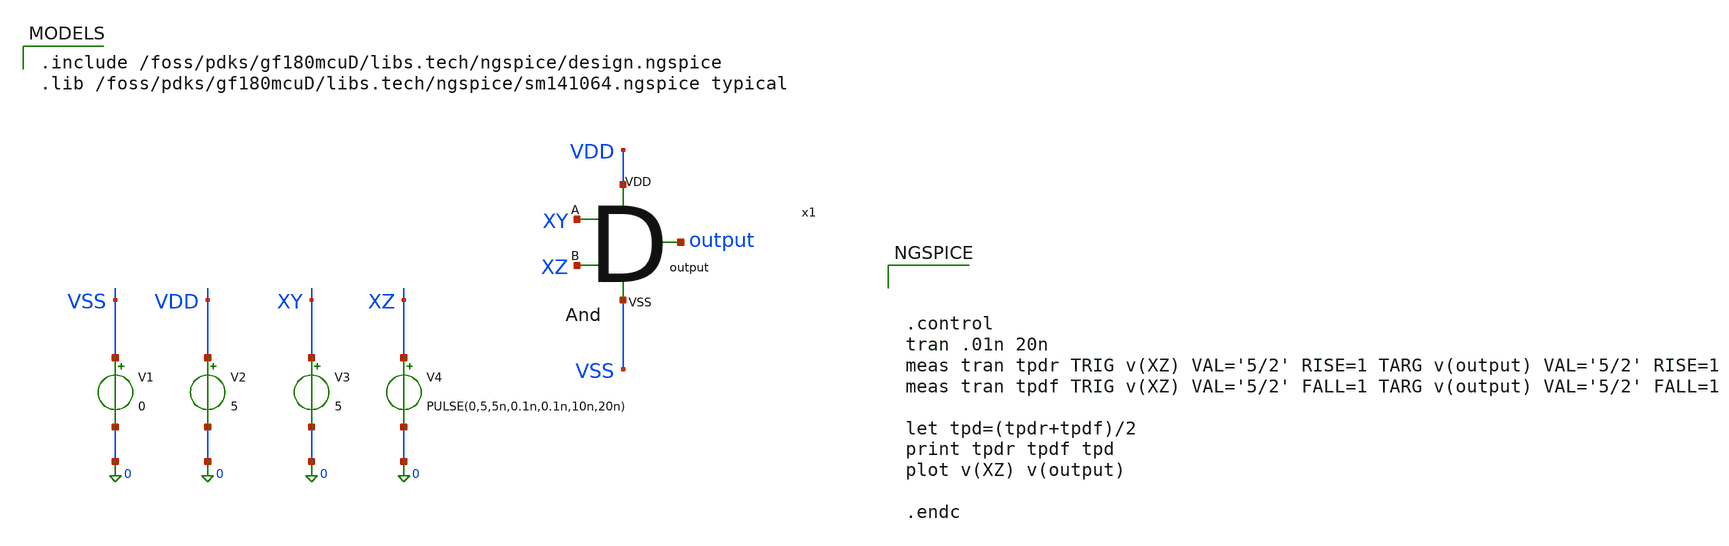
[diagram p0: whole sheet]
** sch_path: activities/opamp3AKAM/xDelayTB.sch
**.subckt xDelayTB
V1 VSS 0 0
V2 VDD 0 5
V3 XY 0 5
V4 XZ 0 PULSE(0,5,5n,0.1n,0.1n,10n,20n)
x1 XY VDD XZ output VSS andGate
**** begin user architecture code

.include /foss/pdks/gf180mcuD/libs.tech/ngspice/design.ngspice
.lib /foss/pdks/gf180mcuD/libs.tech/ngspice/sm141064.ngspice typical




.control
tran .01n 20n
meas tran tpdr TRIG v(XZ) VAL='5/2' RISE=1 TARG v(output) VAL='5/2' RISE=1
meas tran tpdf TRIG v(XZ) VAL='5/2' FALL=1 TARG v(output) VAL='5/2' FALL=1

let tpd=(tpdr+tpdf)/2
print tpdr tpdf tpd
plot v(XZ) v(output)

.endc


**** end user architecture code
**.ends
.end
